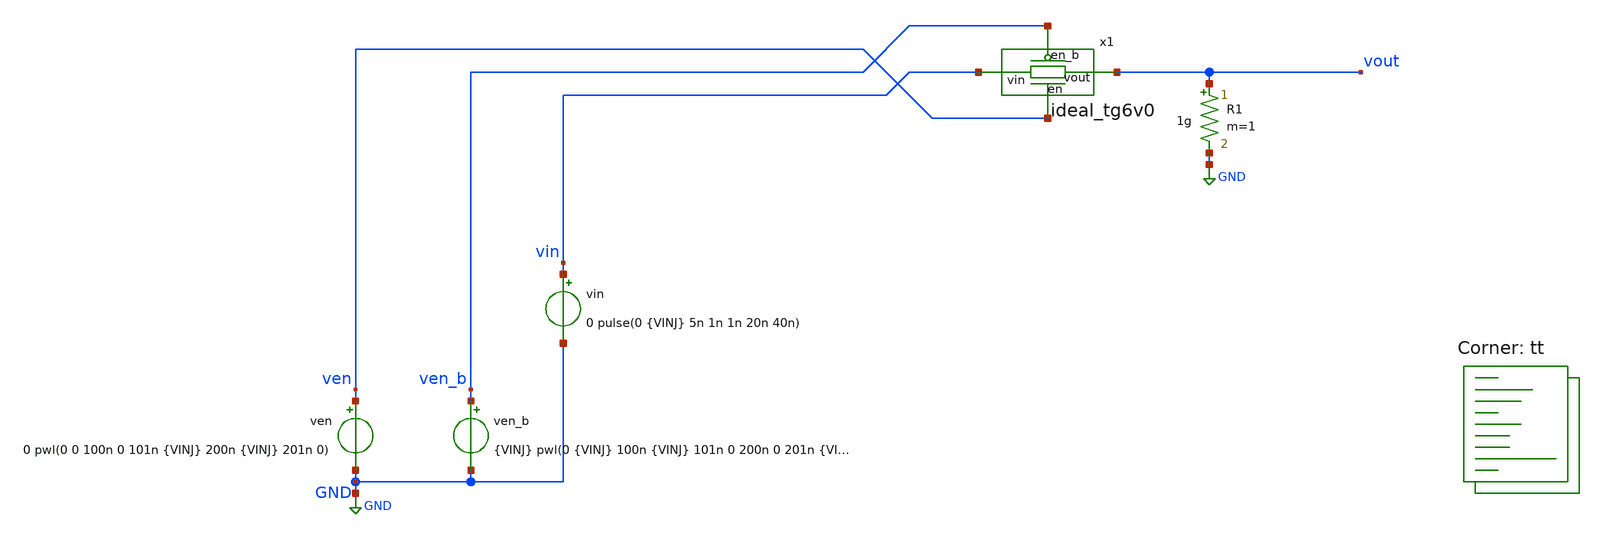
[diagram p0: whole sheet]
** sch_path: xschem/test_tg6v0.sch
**.subckt test_tg6v0
ven ven GND 0 pwl(0 0 100n 0 101n {VINJ} 200n {VINJ} 201n 0)
vin vin GND 0 pulse(0 {VINJ} 5n 1n 1n 20n 40n)
R1 vout GND 1g m=1
x1 vin vout ven ven_b ideal_tg6v0
ven_b ven_b GND {VINJ} pwl(0 {VINJ} 100n {VINJ} 101n 0 200n 0 201n {VINJ})
**** begin user architecture code
.lib $::SKYWATER_MODELS/sky130.lib.spice tt



* .options reltol=0.0001 abstol=10e-15
.param VINJ=6
.param VSS=0
.options savecurrents
.control
  save all
  op
  remzerovec
  write test_tg6v0.raw
  set appendwrite
  * vb sweep
  *dc v1 0 6 0.2 vb 0 6 1
  *remzerovec
  *write test_tg6v0.raw
  * dc sweep
  *dc v1 0 6 0.1
  *remzerovec
  *write test_tg6v0.raw
  * tran
  tran 100p 300n
  remzerovec
  write test_tg6v0.raw
.endc



**** end user architecture code
**.ends

* expanding   symbol:  ideal_tg6v0.sym # of pins=4
** sym_path: xschem/ideal_tg6v0.sym
** sch_path: xschem/ideal_tg6v0.sch
.subckt ideal_tg6v0 vin vout en en_b
*.ipin vin
*.ipin en_b
*.opin vout
*.ipin en
**** begin user architecture code


.model sw_vinj SW vt=3 vh=0.1 ron=14k roff=10gig
.model sw_1v8 SW vt={1.8/2}  vh=0.1 ron=10k roff=10gig


**** end user architecture code
S1 vin vout en en_b sw_vinj
.ends

.GLOBAL GND
.end
